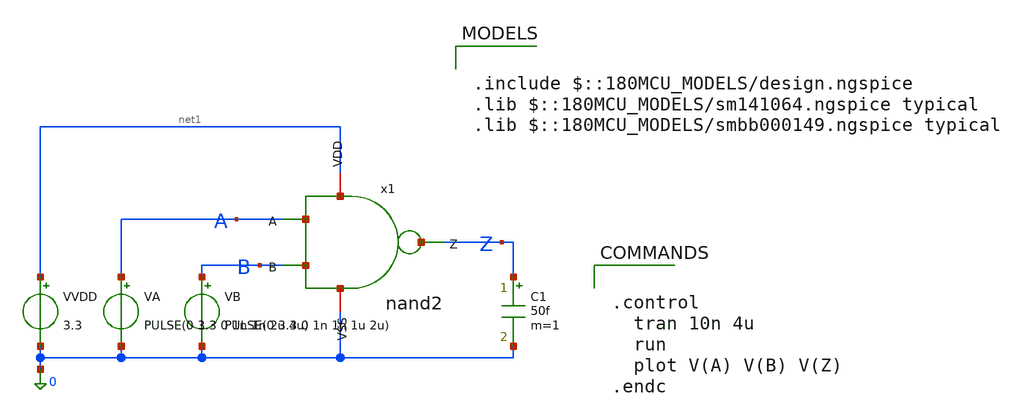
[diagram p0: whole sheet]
** sch_path: sar_logic/sar_designs/tb_nand2.sch
**.subckt tb_nand2
x1 net1 Z A B 0 nand2
VB B 0 PULSE(0 3.3 0 1n 1n 1u 2u)
VA A 0 PULSE(0 3.3 0 1n 1n 2u 4u)
VVDD net1 0 3.3
C1 Z 0 50f m=1
**** begin user architecture code

.include $::180MCU_MODELS/design.ngspice
.lib $::180MCU_MODELS/sm141064.ngspice typical
.lib $::180MCU_MODELS/smbb000149.ngspice typical



.control
  tran 10n 4u
  run
  plot V(A) V(B) V(Z)
.endc


**** end user architecture code
**.ends

* expanding   symbol:  nand2.sym # of pins=5
** sym_path: sar_logic/sar_designs/nand2.sym
** sch_path: sar_logic/sar_designs/nand2.sch
.subckt nand2 VDD Z A B VSS
*.ipin A
*.ipin B
*.iopin VSS
*.iopin VDD
*.opin Z
XM1 Z A VDD VDD pfet_03v3 L=0.28u W=1u nf=1 ad='int((nf+1)/2) * W/nf * 0.18u' as='int((nf+2)/2) * W/nf * 0.18u'
+ pd='2*int((nf+1)/2) * (W/nf + 0.18u)' ps='2*int((nf+2)/2) * (W/nf + 0.18u)' nrd='0.18u / W' nrs='0.18u / W'
+ sa=0 sb=0 sd=0 m=1
XM2 Z B VDD VDD pfet_03v3 L=0.28u W=1u nf=1 ad='int((nf+1)/2) * W/nf * 0.18u' as='int((nf+2)/2) * W/nf * 0.18u'
+ pd='2*int((nf+1)/2) * (W/nf + 0.18u)' ps='2*int((nf+2)/2) * (W/nf + 0.18u)' nrd='0.18u / W' nrs='0.18u / W'
+ sa=0 sb=0 sd=0 m=1
XM3 Z A net1 VSS nfet_03v3 L=0.28u W=1u nf=1 ad='int((nf+1)/2) * W/nf * 0.18u' as='int((nf+2)/2) * W/nf * 0.18u'
+ pd='2*int((nf+1)/2) * (W/nf + 0.18u)' ps='2*int((nf+2)/2) * (W/nf + 0.18u)' nrd='0.18u / W' nrs='0.18u / W'
+ sa=0 sb=0 sd=0 m=1
XM4 net1 B VSS VSS nfet_03v3 L=0.28u W=1u nf=1 ad='int((nf+1)/2) * W/nf * 0.18u' as='int((nf+2)/2) * W/nf * 0.18u'
+ pd='2*int((nf+1)/2) * (W/nf + 0.18u)' ps='2*int((nf+2)/2) * (W/nf + 0.18u)' nrd='0.18u / W' nrs='0.18u / W'
+ sa=0 sb=0 sd=0 m=1
.ends

.end
